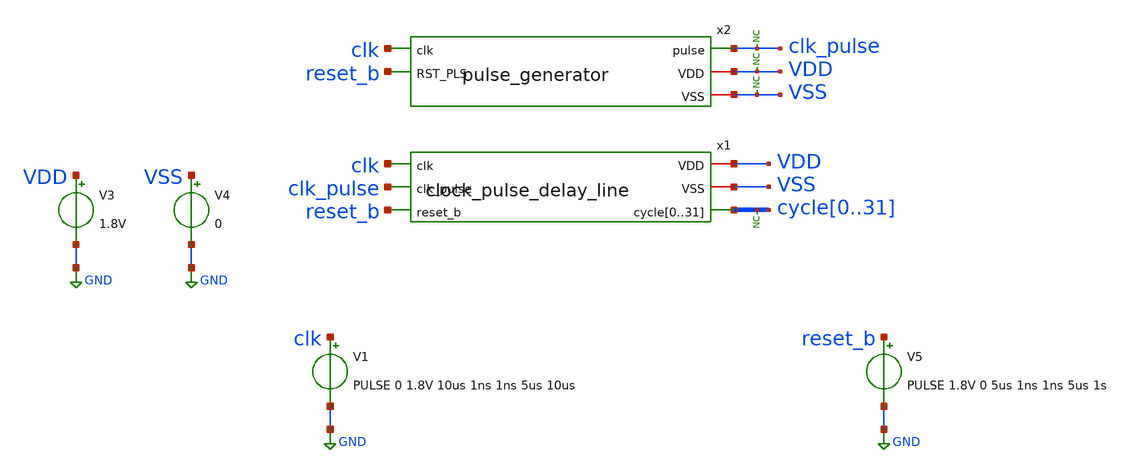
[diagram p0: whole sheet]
** sch_path: xschem/tests/clock_pulse_delay_line/pulse_generator and_delay_line_test.sch
**.subckt pulse_generator and_delay_line_test
V3 VDD GND 1.8V
V4 VSS GND 0
x1 clk VDD VSS clk_pulse reset_b cycle0 cycle1 cycle2 cycle3 cycle4 cycle5 cycle6 cycle7 cycle8
+ cycle9 cycle10 cycle11 cycle12 cycle13 cycle14 cycle15 cycle16 cycle17 cycle18 cycle19 cycle20 cycle21
+ cycle22 cycle23 cycle24 cycle25 cycle26 cycle27 cycle28 cycle29 cycle30 cycle31 clock_pulse_delay_line
* noconn cycle[0..31]
V1 clk GND PULSE 0 1.8V 10us 1ns 1ns 5us 10us
V5 reset_b GND PULSE 1.8V 0 5us 1ns 1ns 5us 1s
* noconn clk_pulse
* noconn VDD
* noconn VSS
x2 clk clk_pulse VDD VSS reset_b pulse_generator
**** begin user architecture code
 .lib $::SKYWATER_MODELS/sky130.lib.spice tt
.include $::SKYWATER_STDCELLS/sky130_fd_sc_hd.spice


.options acct list
.temp 25
*vvcc VDD 0 dc 1.8
*vvss VSS 0 0
.control
tran 0.1u 350u
*plot RST_PLS clk+2 Pulse+4
plot reset_b-6 clk-4 clk_pulse-2 cycle0 cycle1+2 cycle2+4 cycle3+6 cycle4+8 cycle5+10 cycle6+12
+ cycle7+14 cycle8+16 cycle9+18 cycle10+20 cycle11+22 cycle12+24 cycle13+26 cycle14+28 cycle15+30 cycle16+32
+ cycle17+34 cycle18+36 cycle19+38 cycle20+40 cycle21+42 cycle22+44  cycle23+46 cycle24+48 cycle25+50 cycle26+52
+ cycle27+54 cycle28+56 cycle29+58 cycle30+60 cycle31+62

write pulse_generator_and_delay_line.raw
.endc


**** end user architecture code
**.ends

* expanding   symbol:  src/clock_pulse_delay_line/clock_pulse_delay_line.sym # of pins=6
** sym_path: xschem/src/clock_pulse_delay_line/clock_pulse_delay_line.sym
** sch_path: xschem/src/clock_pulse_delay_line/clock_pulse_delay_line.sch
.subckt clock_pulse_delay_line clk VDD VSS clk_pulse reset_b cycle0 cycle1 cycle2 cycle3 cycle4
+ cycle5 cycle6 cycle7 cycle8 cycle9 cycle10 cycle11 cycle12 cycle13 cycle14 cycle15 cycle16 cycle17 cycle18
+ cycle19 cycle20 cycle21 cycle22 cycle23 cycle24 cycle25 cycle26 cycle27 cycle28 cycle29 cycle30 cycle31
*.ipin clk_pulse
*.opin
*+ cycle0,cycle1,cycle2,cycle3,cycle4,cycle5,cycle6,cycle7,cycle8,cycle9,cycle10,cycle11,cycle12,cycle13,cycle14,cycle15,cycle16,cycle17,cycle18,cycle19,cycle20,cycle21,cycle22,cycle23,cycle24,cycle25,cycle26,cycle27,cycle28,cycle29,cycle30,cycle31
*.iopin VSS
*.iopin VDD
*.ipin clk
*.ipin reset_b
* noconn cycle31
x3 clk clk_pulse reset_b VSS VSS VDD VDD cycle1 sky130_fd_sc_hd__dfrtn_1
x1 clk cycle1 reset_b VSS VSS VDD VDD cycle2 sky130_fd_sc_hd__dfrtn_1
x24 clk cycle2 reset_b VSS VSS VDD VDD cycle3 sky130_fd_sc_hd__dfrtn_1
x26 clk cycle3 reset_b VSS VSS VDD VDD cycle4 sky130_fd_sc_hd__dfrtn_1
x28 clk cycle4 reset_b VSS VSS VDD VDD cycle5 sky130_fd_sc_hd__dfrtn_1
x21 clk cycle5 reset_b VSS VSS VDD VDD cycle6 sky130_fd_sc_hd__dfrtn_1
x23 clk cycle6 reset_b VSS VSS VDD VDD cycle7 sky130_fd_sc_hd__dfrtn_1
x25 clk cycle7 reset_b VSS VSS VDD VDD cycle8 sky130_fd_sc_hd__dfrtn_1
x27 clk cycle8 reset_b VSS VSS VDD VDD cycle9 sky130_fd_sc_hd__dfrtn_1
x29 clk cycle9 reset_b VSS VSS VDD VDD cycle10 sky130_fd_sc_hd__dfrtn_1
x30 clk cycle10 reset_b VSS VSS VDD VDD cycle11 sky130_fd_sc_hd__dfrtn_1
x31 clk cycle11 reset_b VSS VSS VDD VDD cycle12 sky130_fd_sc_hd__dfrtn_1
x32 clk cycle12 reset_b VSS VSS VDD VDD cycle13 sky130_fd_sc_hd__dfrtn_1
x4 clk cycle13 reset_b VSS VSS VDD VDD cycle14 sky130_fd_sc_hd__dfrtn_1
x5 clk cycle15 reset_b VSS VSS VDD VDD cycle16 sky130_fd_sc_hd__dfrtn_1
x6 clk cycle16 reset_b VSS VSS VDD VDD cycle17 sky130_fd_sc_hd__dfrtn_1
x7 clk cycle17 reset_b VSS VSS VDD VDD cycle18 sky130_fd_sc_hd__dfrtn_1
x8 clk cycle18 reset_b VSS VSS VDD VDD cycle19 sky130_fd_sc_hd__dfrtn_1
x9 clk cycle19 reset_b VSS VSS VDD VDD cycle20 sky130_fd_sc_hd__dfrtn_1
x10 clk cycle20 reset_b VSS VSS VDD VDD cycle21 sky130_fd_sc_hd__dfrtn_1
x11 clk cycle21 reset_b VSS VSS VDD VDD cycle22 sky130_fd_sc_hd__dfrtn_1
x12 clk cycle22 reset_b VSS VSS VDD VDD cycle23 sky130_fd_sc_hd__dfrtn_1
x13 clk cycle23 reset_b VSS VSS VDD VDD cycle24 sky130_fd_sc_hd__dfrtn_1
x14 clk cycle24 reset_b VSS VSS VDD VDD cycle25 sky130_fd_sc_hd__dfrtn_1
x15 clk cycle25 reset_b VSS VSS VDD VDD cycle26 sky130_fd_sc_hd__dfrtn_1
x16 clk cycle26 reset_b VSS VSS VDD VDD cycle27 sky130_fd_sc_hd__dfrtn_1
x17 clk cycle27 reset_b VSS VSS VDD VDD cycle28 sky130_fd_sc_hd__dfrtn_1
x18 clk cycle28 reset_b VSS VSS VDD VDD cycle29 sky130_fd_sc_hd__dfrtn_1
x19 clk cycle29 reset_b VSS VSS VDD VDD cycle30 sky130_fd_sc_hd__dfrtn_1
x20 clk cycle30 reset_b VSS VSS VDD VDD cycle31 sky130_fd_sc_hd__dfrtn_1
x2 clk cycle14 reset_b VSS VSS VDD VDD cycle15 sky130_fd_sc_hd__dfrtn_1
x33 clk_pulse VSS VSS VDD VDD cycle0 sky130_fd_sc_hd__buf_12
.ends


* expanding   symbol:  src/pulse_generator/pulse_generator.sym # of pins=5
** sym_path: xschem/src/pulse_generator/pulse_generator.sym
** sch_path: xschem/src/pulse_generator/pulse_generator.sch
.subckt pulse_generator clk pulse VDD VSS RST_PLS
*.ipin clk
*.ipin RST_PLS
*.opin pulse
*.iopin VDD
*.iopin VSS
x1 clk net1 RST_PLS VSS VSS VDD VDD clk2 net1 sky130_fd_sc_hd__dfrbp_1
x2 clk2 net2 RST_PLS VSS VSS VDD VDD clk4 net2 sky130_fd_sc_hd__dfrbp_1
x3 clk4 net3 RST_PLS VSS VSS VDD VDD clk8 net3 sky130_fd_sc_hd__dfrbp_1
x4 clk8 net4 RST_PLS VSS VSS VDD VDD clk16 net4 sky130_fd_sc_hd__dfrbp_1
x5 delayed clk64 VSS VSS VDD VDD net7 sky130_fd_sc_hd__xor2_1
x9 clk16 net5 RST_PLS VSS VSS VDD VDD clk32 net5 sky130_fd_sc_hd__dfrbp_1
x10 clk32 net6 RST_PLS VSS VSS VDD VDD clk64 net6 sky130_fd_sc_hd__dfrbp_1
* noconn pulse
x6 clk clk64 RST_PLS VSS VSS VDD VDD delayed sky130_fd_sc_hd__dfrtp_1
x7 clk net7 RST_PLS VSS VSS VDD VDD pulse sky130_fd_sc_hd__dfrtn_1
.ends

.GLOBAL GND
.end
